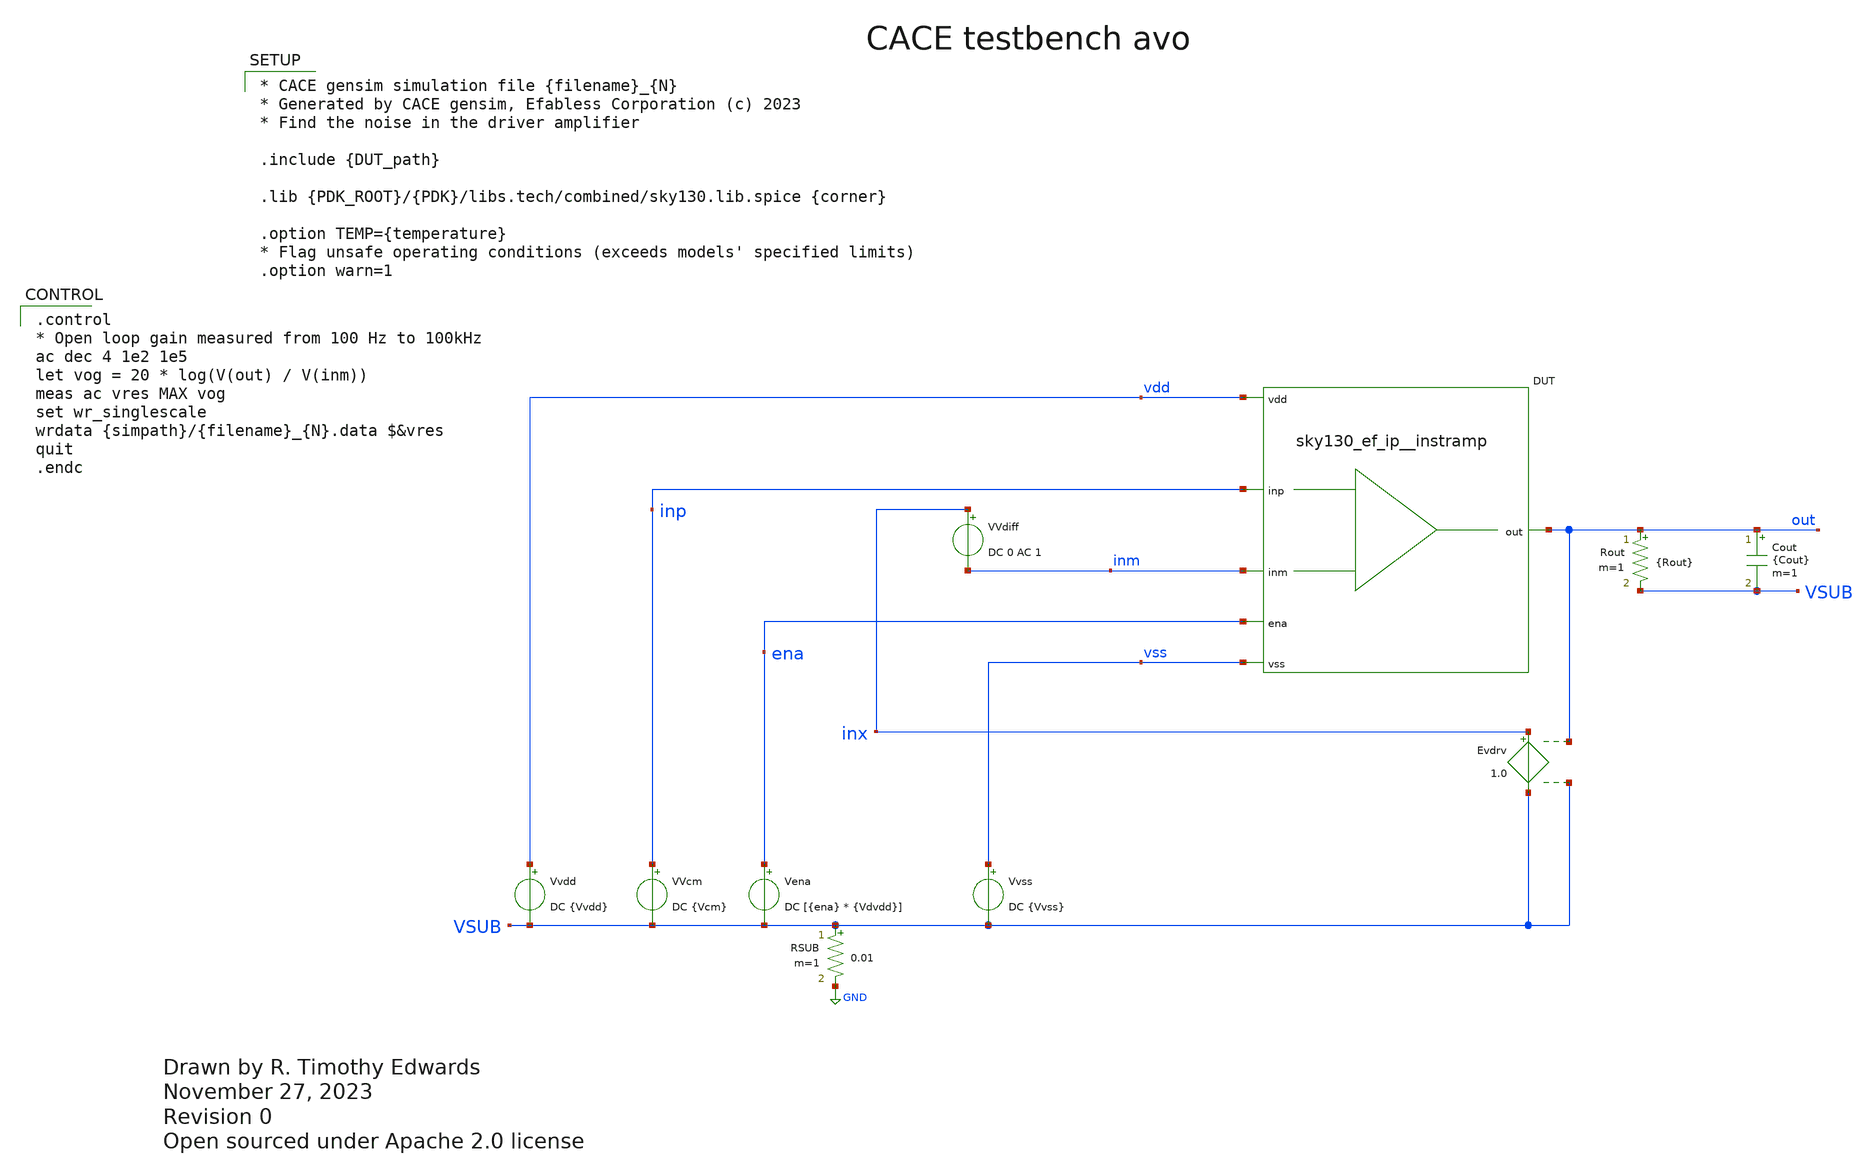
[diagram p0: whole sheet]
** sch_path: cace/avo.sch
* Open sourced under Apache 2.0 license
**.subckt avo
VVcm inp VSUB DC {Vcm}
Vena ena VSUB DC [{ena} * {Vdvdd}]
Vvss vss VSUB DC {Vvss}
Rout out VSUB {Rout} m=1
Cout out VSUB {Cout} m=1
Vvdd vdd VSUB DC {Vvdd}
RSUB VSUB GND 0.01 m=1
XDUT {PIN|vdd|vdd} {PIN|vss|vss} {PIN|inm|inm} {PIN|inp|inp} {PIN|out|out} {PIN|ena|ena} {DUT_name}
Evdrv inx VSUB out VSUB 1.0
VVdiff inx inm DC 0 AC 1
**** begin user architecture code

.control
* Open loop gain measured from 100 Hz to 100kHz
ac dec 4 1e2 1e5
let vog = 20 * log(V(out) / V(inm))
meas ac vres MAX vog
set wr_singlescale
wrdata {simpath}/{filename}_{N}.data $&vres
quit
.endc



* CACE gensim simulation file {filename}_{N}
* Generated by CACE gensim, Efabless Corporation (c) 2023
* Find the noise in the driver amplifier

.include {DUT_path}

.lib {PDK_ROOT}/{PDK}/libs.tech/combined/sky130.lib.spice {corner}

.option TEMP={temperature}
* Flag unsafe operating conditions (exceeds models' specified limits)
.option warn=1


**** end user architecture code
**.ends
.GLOBAL GND
.end
